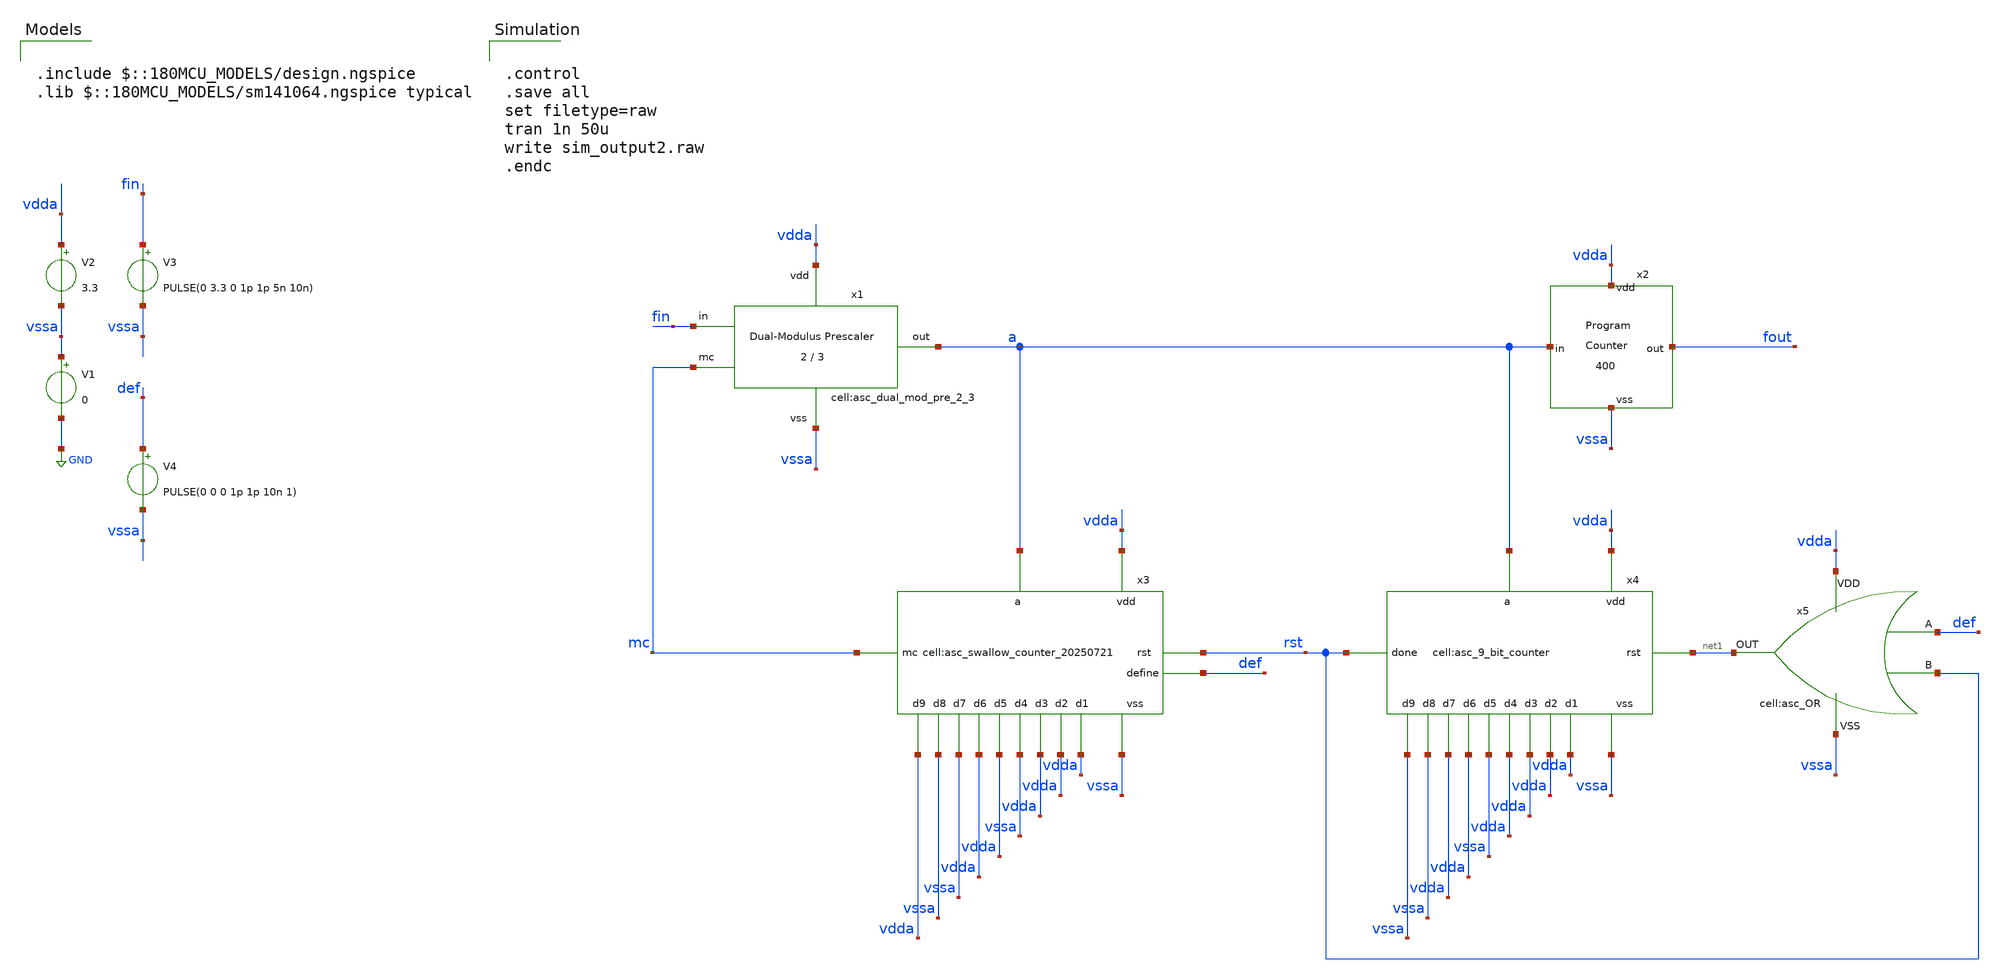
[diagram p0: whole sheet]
** sch_path: designs/libs/xp_tb_analog/tb_pulse_swallow_divider_20250721/tb_pulse_swallow_divider_20250721.sch
**.subckt tb_pulse_swallow_divider_20250721
V1 vssa GND 0
V2 vdda vssa 3.3
V3 fin vssa PULSE(0 3.3 0 1p 1p 5n 10n)
x1 vdda vssa a fin mc asc_dual_mod_pre_2_3
x2 a fout vdda vssa asc_program_counter_400
x3 mc vdda vssa vssa vdda vdda vssa vdda vdda vdda vssa rst vdda a def asc_swallow_counter_20250721
x4 rst vssa vssa vdda vdda vssa vdda vdda vdda vdda vssa net1 vdda a asc_9_bit_counter
x5 vdda vssa net1 def rst asc_OR
V4 def vssa PULSE(0 0 0 1p 1p 10n 1)
**** begin user architecture code

.include $::180MCU_MODELS/design.ngspice
.lib $::180MCU_MODELS/sm141064.ngspice typical



.control
.save all
set filetype=raw
tran 1n 50u
write sim_output2.raw
.endc


**** end user architecture code
**.ends
.GLOBAL GND
.end
